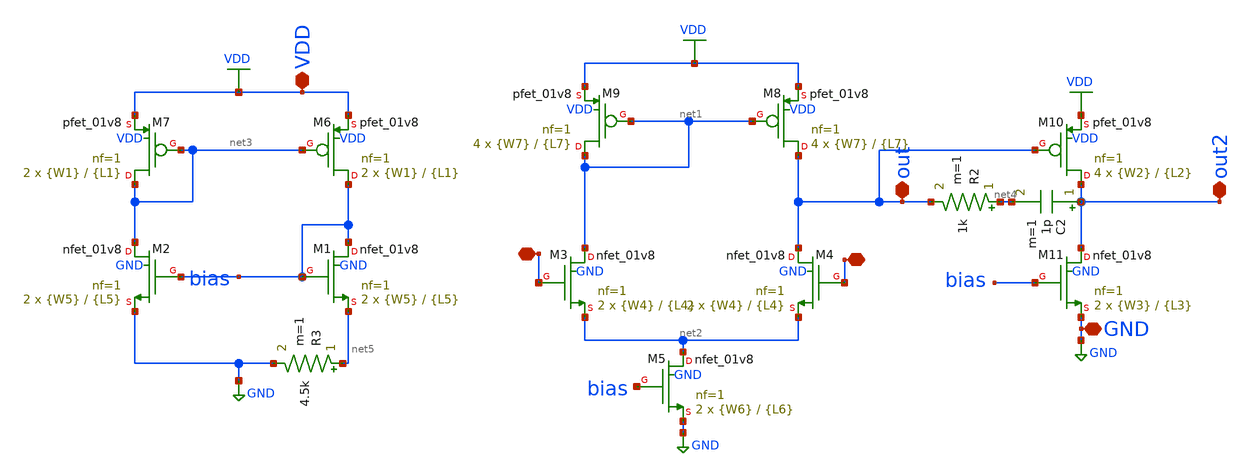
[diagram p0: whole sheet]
** sch_path: xschem/op4.sch
**.subckt op4 VDD GND - + out out2
*.iopin VDD
*.iopin GND
*.iopin -
*.iopin +
*.iopin out
*.iopin out2
C2 out2 net4 1p m=1
R2 net4 out 1k m=1
XM1 bias bias net5 GND sky130_fd_pr__nfet_01v8 L={L5} W={W5} nf=1 ad='int((nf+1)/2) * W/nf * 0.29' as='int((nf+2)/2) * W/nf * 0.29'
+ pd='2*int((nf+1)/2) * (W/nf + 0.29)' ps='2*int((nf+2)/2) * (W/nf + 0.29)' nrd='0.29 / W' nrs='0.29 / W'
+ sa=0 sb=0 sd=0 mult=2 m=2
XM2 net3 bias GND GND sky130_fd_pr__nfet_01v8 L={L5} W={W5} nf=1 ad='int((nf+1)/2) * W/nf * 0.29' as='int((nf+2)/2) * W/nf * 0.29'
+ pd='2*int((nf+1)/2) * (W/nf + 0.29)' ps='2*int((nf+2)/2) * (W/nf + 0.29)' nrd='0.29 / W' nrs='0.29 / W'
+ sa=0 sb=0 sd=0 mult=2 m=2
XM3 net1 - net2 GND sky130_fd_pr__nfet_01v8 L={L4} W={W4} nf=1 ad='int((nf+1)/2) * W/nf * 0.29' as='int((nf+2)/2) * W/nf * 0.29'
+ pd='2*int((nf+1)/2) * (W/nf + 0.29)' ps='2*int((nf+2)/2) * (W/nf + 0.29)' nrd='0.29 / W' nrs='0.29 / W'
+ sa=0 sb=0 sd=0 mult=2 m=2
XM4 out + net2 GND sky130_fd_pr__nfet_01v8 L={L4} W={W4} nf=1 ad='int((nf+1)/2) * W/nf * 0.29' as='int((nf+2)/2) * W/nf * 0.29'
+ pd='2*int((nf+1)/2) * (W/nf + 0.29)' ps='2*int((nf+2)/2) * (W/nf + 0.29)' nrd='0.29 / W' nrs='0.29 / W'
+ sa=0 sb=0 sd=0 mult=2 m=2
XM6 bias net3 VDD VDD sky130_fd_pr__pfet_01v8 L={L1} W={W1} nf=1 ad='int((nf+1)/2) * W/nf * 0.29' as='int((nf+2)/2) * W/nf * 0.29'
+ pd='2*int((nf+1)/2) * (W/nf + 0.29)' ps='2*int((nf+2)/2) * (W/nf + 0.29)' nrd='0.29 / W' nrs='0.29 / W'
+ sa=0 sb=0 sd=0 mult=2 m=2
XM7 net3 net3 VDD VDD sky130_fd_pr__pfet_01v8 L={L1} W={W1} nf=1 ad='int((nf+1)/2) * W/nf * 0.29' as='int((nf+2)/2) * W/nf * 0.29'
+ pd='2*int((nf+1)/2) * (W/nf + 0.29)' ps='2*int((nf+2)/2) * (W/nf + 0.29)' nrd='0.29 / W' nrs='0.29 / W'
+ sa=0 sb=0 sd=0 mult=2 m=2
XM8 out net1 VDD VDD sky130_fd_pr__pfet_01v8 L={L7} W={W7} nf=1 ad='int((nf+1)/2) * W/nf * 0.29' as='int((nf+2)/2) * W/nf * 0.29'
+ pd='2*int((nf+1)/2) * (W/nf + 0.29)' ps='2*int((nf+2)/2) * (W/nf + 0.29)' nrd='0.29 / W' nrs='0.29 / W'
+ sa=0 sb=0 sd=0 mult=4 m=4
XM9 net1 net1 VDD VDD sky130_fd_pr__pfet_01v8 L={L7} W={W7} nf=1 ad='int((nf+1)/2) * W/nf * 0.29' as='int((nf+2)/2) * W/nf * 0.29'
+ pd='2*int((nf+1)/2) * (W/nf + 0.29)' ps='2*int((nf+2)/2) * (W/nf + 0.29)' nrd='0.29 / W' nrs='0.29 / W'
+ sa=0 sb=0 sd=0 mult=4 m=4
XM5 net2 bias GND GND sky130_fd_pr__nfet_01v8 L={L6} W={W6} nf=1 ad='int((nf+1)/2) * W/nf * 0.29' as='int((nf+2)/2) * W/nf * 0.29'
+ pd='2*int((nf+1)/2) * (W/nf + 0.29)' ps='2*int((nf+2)/2) * (W/nf + 0.29)' nrd='0.29 / W' nrs='0.29 / W'
+ sa=0 sb=0 sd=0 mult=2 m=2
XM10 out2 out VDD VDD sky130_fd_pr__pfet_01v8 L={L2} W={W2} nf=1 ad='int((nf+1)/2) * W/nf * 0.29' as='int((nf+2)/2) * W/nf * 0.29'
+ pd='2*int((nf+1)/2) * (W/nf + 0.29)' ps='2*int((nf+2)/2) * (W/nf + 0.29)' nrd='0.29 / W' nrs='0.29 / W'
+ sa=0 sb=0 sd=0 mult=4 m=4
XM11 out2 bias GND GND sky130_fd_pr__nfet_01v8 L={L3} W={W3} nf=1 ad='int((nf+1)/2) * W/nf * 0.29' as='int((nf+2)/2) * W/nf * 0.29'
+ pd='2*int((nf+1)/2) * (W/nf + 0.29)' ps='2*int((nf+2)/2) * (W/nf + 0.29)' nrd='0.29 / W' nrs='0.29 / W'
+ sa=0 sb=0 sd=0 mult=2 m=2
R3 net5 GND 4.5k m=1
**** begin user architecture code


**************
*PMOS cms
.param L1=40
.param W1=1

**************
*NMOS cms
.param L5=20
.param W5=1

**************
*PMOS differential
.param L7=10
.param W7=0.5

**************
*differential Pair
.param L4=10
.param W4=1.5

**************
*NMOS current control
.param L6=5
.param W6=1

**************
*Second Stage
.param L2=30
.param W2=1

**************
*NMOS current second stage
.param L3=20
.param W3=0.5


**** end user architecture code
**.ends
.GLOBAL VDD
.GLOBAL GND
.end
